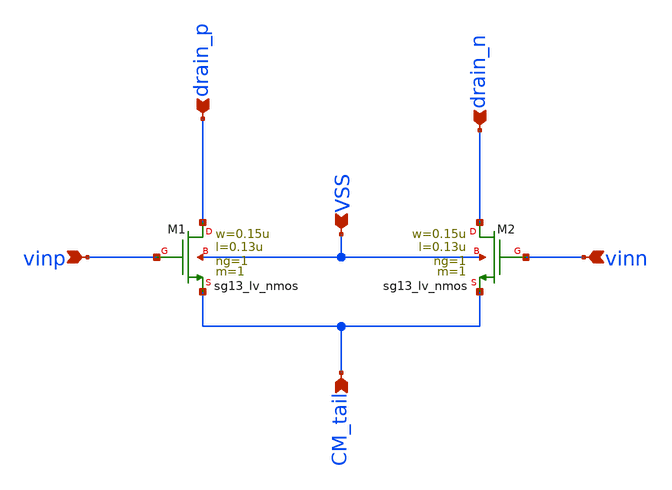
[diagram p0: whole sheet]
** sch_path: analog-db/templates/miscellaneous/diff_pair_nmos.sch
**.subckt diff_pair_nmos vinp vinn CM_tail drain_n drain_p VSS
*.ipin vinp
*.ipin vinn
*.ipin CM_tail
*.ipin drain_n
*.ipin drain_p
*.ipin VSS
XM1 drain_p vinp CM_tail VSS sg13_lv_nmos w=0.15u l=0.13u ng=1 m=1 mm_ok=1
XM2 drain_n vinn CM_tail VSS sg13_lv_nmos w=0.15u l=0.13u ng=1 m=1 mm_ok=1
**.ends
.end
